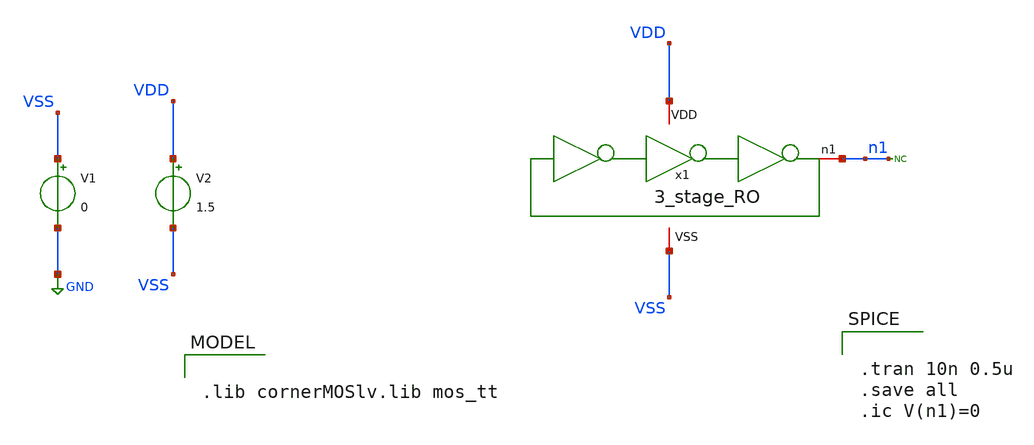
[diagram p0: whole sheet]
** sch_path: Lab2/3_stage_RO_tb_tran.sch
**.subckt 3_stage_RO_tb_tran
V1 VSS GND 0
V2 VDD VSS 1.5
* noconn n1
x1 VDD VSS n1 3_stage_RO
**** begin user architecture code


.tran 10n 0.5u
.save all
.ic V(n1)=0



.lib cornerMOSlv.lib mos_tt

**** end user architecture code
**.ends

* expanding   symbol:
*+  /home/fcastellanos/Documents/SEED_Bootcamp_ihp/Modulo_Analogico/Lab2/3_stage_RO.sym # of pins=3
** sym_path: /home/fcastellanos/Documents/SEED_Bootcamp_ihp/Modulo_Analogico/Lab2/3_stage_RO.sym
** sch_path: /home/fcastellanos/Documents/SEED_Bootcamp_ihp/Modulo_Analogico/Lab2/3_stage_RO.sch
.subckt 3_stage_RO VDD VSS n1
*.iopin VDD
*.iopin VSS
*.iopin n1
x1 n1 VDD VSS n2 inverter
x2 n2 VDD VSS n3 inverter
x3 n3 VDD VSS n1 inverter
.ends

.GLOBAL GND
.end
